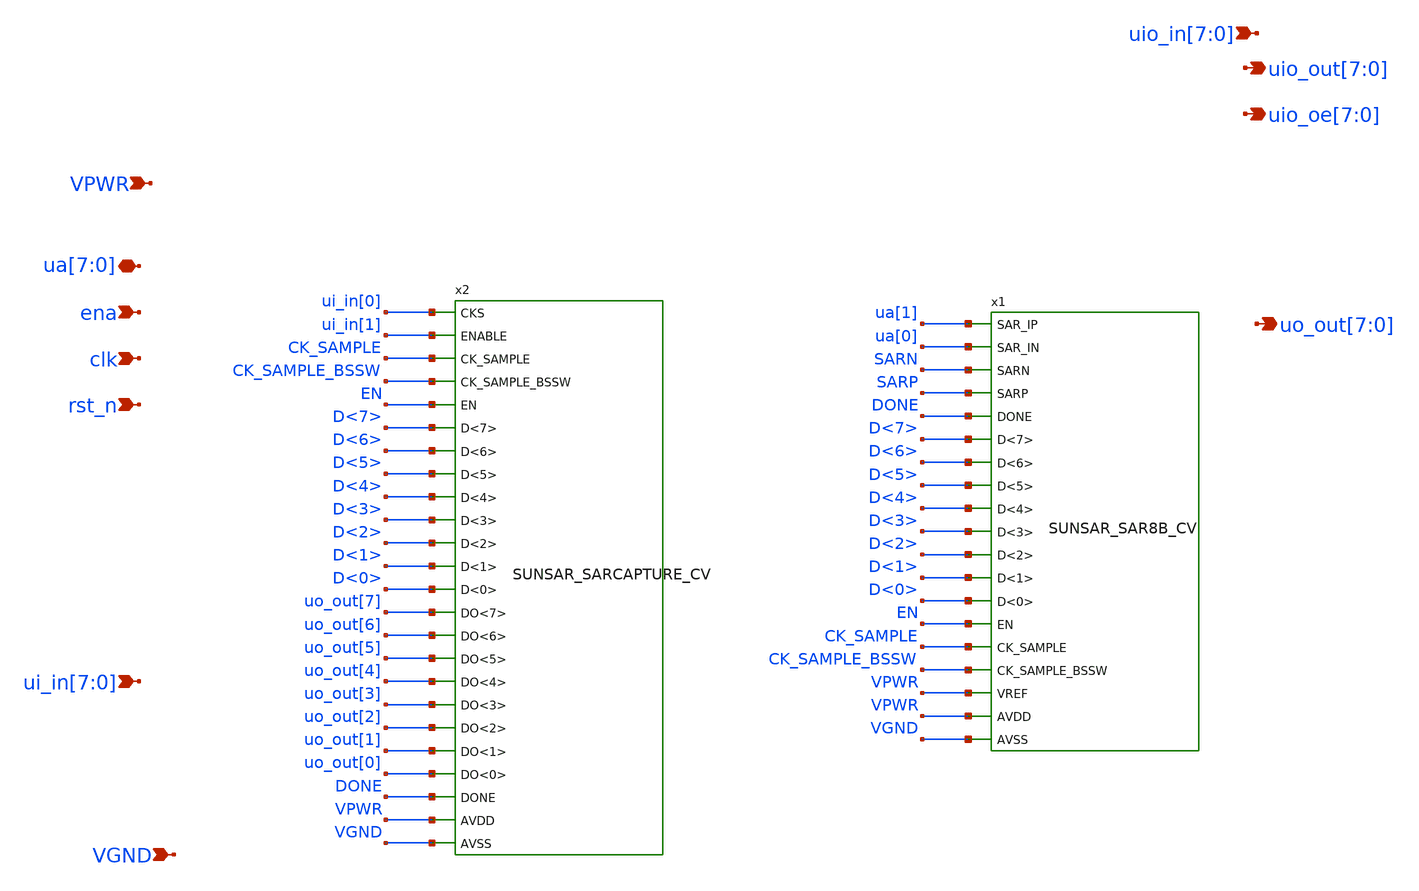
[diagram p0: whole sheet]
** sch_path: ip/tt06_sar_sky130nm/design/TT06_SAR_SKY130NM/tt_um_TT06_SAR_wulffern.sch
**.subckt tt_um_TT06_SAR_wulffern VPWR VGND
*+ ui_in[7],ui_in[6],ui_in[5],ui_in[4],ui_in[3],ui_in[2],ui_in[1],ui_in[0] uo_out[7],uo_out[6],uo_out[5],uo_out[4],uo_out[3],uo_out[2],uo_out[1],uo_out[0]
*+ uio_in[7],uio_in[6],uio_in[5],uio_in[4],uio_in[3],uio_in[2],uio_in[1],uio_in[0] uio_out[7],uio_out[6],uio_out[5],uio_out[4],uio_out[3],uio_out[2],uio_out[1],uio_out[0]
*+ uio_oe[7],uio_oe[6],uio_oe[5],uio_oe[4],uio_oe[3],uio_oe[2],uio_oe[1],uio_oe[0] ua[7],ua[6],ua[5],ua[4],ua[3],ua[2],ua[1],ua[0] ena clk rst_n
*.ipin VPWR
*.ipin VGND
*.ipin ui_in[7],ui_in[6],ui_in[5],ui_in[4],ui_in[3],ui_in[2],ui_in[1],ui_in[0]
*.opin uo_out[7],uo_out[6],uo_out[5],uo_out[4],uo_out[3],uo_out[2],uo_out[1],uo_out[0]
*.ipin uio_in[7],uio_in[6],uio_in[5],uio_in[4],uio_in[3],uio_in[2],uio_in[1],uio_in[0]
*.opin uio_out[7],uio_out[6],uio_out[5],uio_out[4],uio_out[3],uio_out[2],uio_out[1],uio_out[0]
*.opin uio_oe[7],uio_oe[6],uio_oe[5],uio_oe[4],uio_oe[3],uio_oe[2],uio_oe[1],uio_oe[0]
*.iopin ua[7],ua[6],ua[5],ua[4],ua[3],ua[2],ua[1],ua[0]
*.ipin ena
*.ipin clk
*.ipin rst_n
x1 ua[1] ua[0] SARN SARP DONE D<7> D<6> D<5> D<4> D<3> D<2> D<1> D<0> EN CK_SAMPLE CK_SAMPLE_BSSW
+ VPWR VPWR VGND SUNSAR_SAR8B_CV
x2 ui_in[0] ui_in[1] CK_SAMPLE CK_SAMPLE_BSSW EN D<7> D<6> D<5> D<4> D<3> D<2> D<1> D<0> uo_out[7]
+ uo_out[6] uo_out[5] uo_out[4] uo_out[3] uo_out[2] uo_out[1] uo_out[0] DONE VPWR VGND SUNSAR_SARCAPTURE_CV
**.ends
.end
